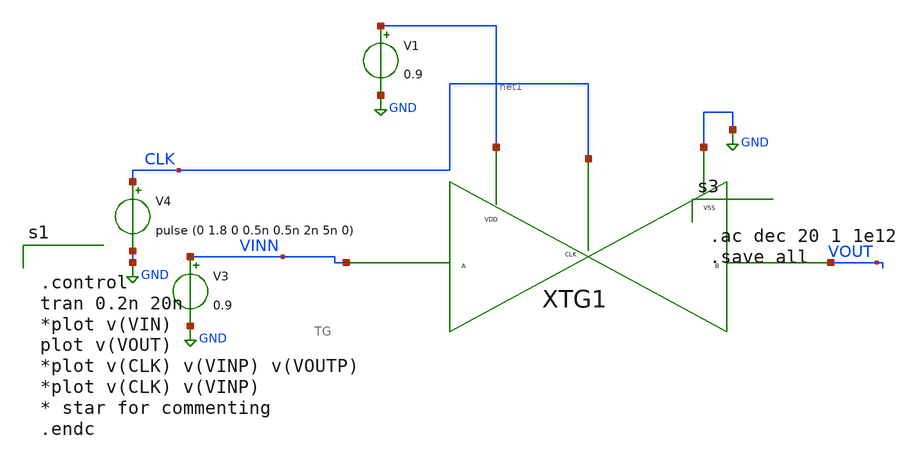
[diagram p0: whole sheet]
** sch_path: xschem/xschem_BGR_Top/Sigma_Delta/Transmission_Gate/Transmission_Gate_TB.sch
**.subckt Transmission_Gate_TB
V3 VINN GND 0.9
V4 CLK GND pulse (0 1.8 0 0.5n 0.5n 2n 5n 0)
XTG1 GND CLK net1 VINN VOUT TG
V1 net1 GND 0.9
**** begin user architecture code


.control
tran 0.2n 20n
*plot v(VIN)
plot v(VOUT)
*plot v(CLK) v(VINP) v(VOUTP)
*plot v(CLK) v(VINP)
* star for commenting
.endc


** opencircuitdesign pdks install
.lib $::SKYWATER_MODELS/sky130.lib.spice tt




.ac dec 20 1 1e12
.save all

**** end user architecture code
**.ends

* expanding   symbol:  Sigma_Delta/Transmission_Gate/TG.sym # of pins=5
** sym_path: xschem/xschem_BGR_Top/Sigma_Delta/Transmission_Gate/TG.sym
** sch_path: xschem/xschem_BGR_Top/Sigma_Delta/Transmission_Gate/TG.sch
.subckt TG VSS CLK VDD A B
*.iopin VDD
*.iopin VSS
*.iopin A
*.iopin B
*.iopin CLK
XM1 A CLK B VSS sky130_fd_pr__nfet_01v8 L=0.15 W=10 nf=1 ad='int((nf+1)/2) * W/nf * 0.29' as='int((nf+2)/2) * W/nf * 0.29'
+ pd='2*int((nf+1)/2) * (W/nf + 0.29)' ps='2*int((nf+2)/2) * (W/nf + 0.29)' nrd='0.29 / W' nrs='0.29 / W'
+ sa=0 sb=0 sd=0 mult=1 m=1
XM2 B CLKB A VDD sky130_fd_pr__pfet_01v8 L=0.15 W=20 nf=2 ad='int((nf+1)/2) * W/nf * 0.29' as='int((nf+2)/2) * W/nf * 0.29'
+ pd='2*int((nf+1)/2) * (W/nf + 0.29)' ps='2*int((nf+2)/2) * (W/nf + 0.29)' nrd='0.29 / W' nrs='0.29 / W'
+ sa=0 sb=0 sd=0 mult=1 m=1
XM3 CLKB CLK VSS VSS sky130_fd_pr__nfet_01v8 L=0.15 W=10 nf=5 ad='int((nf+1)/2) * W/nf * 0.29' as='int((nf+2)/2) * W/nf * 0.29'
+ pd='2*int((nf+1)/2) * (W/nf + 0.29)' ps='2*int((nf+2)/2) * (W/nf + 0.29)' nrd='0.29 / W' nrs='0.29 / W'
+ sa=0 sb=0 sd=0 mult=1 m=1
XM4 CLKB CLK VDD VDD sky130_fd_pr__pfet_01v8 L=0.15 W=20 nf=10 ad='int((nf+1)/2) * W/nf * 0.29' as='int((nf+2)/2) * W/nf * 0.29'
+ pd='2*int((nf+1)/2) * (W/nf + 0.29)' ps='2*int((nf+2)/2) * (W/nf + 0.29)' nrd='0.29 / W' nrs='0.29 / W'
+ sa=0 sb=0 sd=0 mult=1 m=1
.ends

.GLOBAL GND
.end
